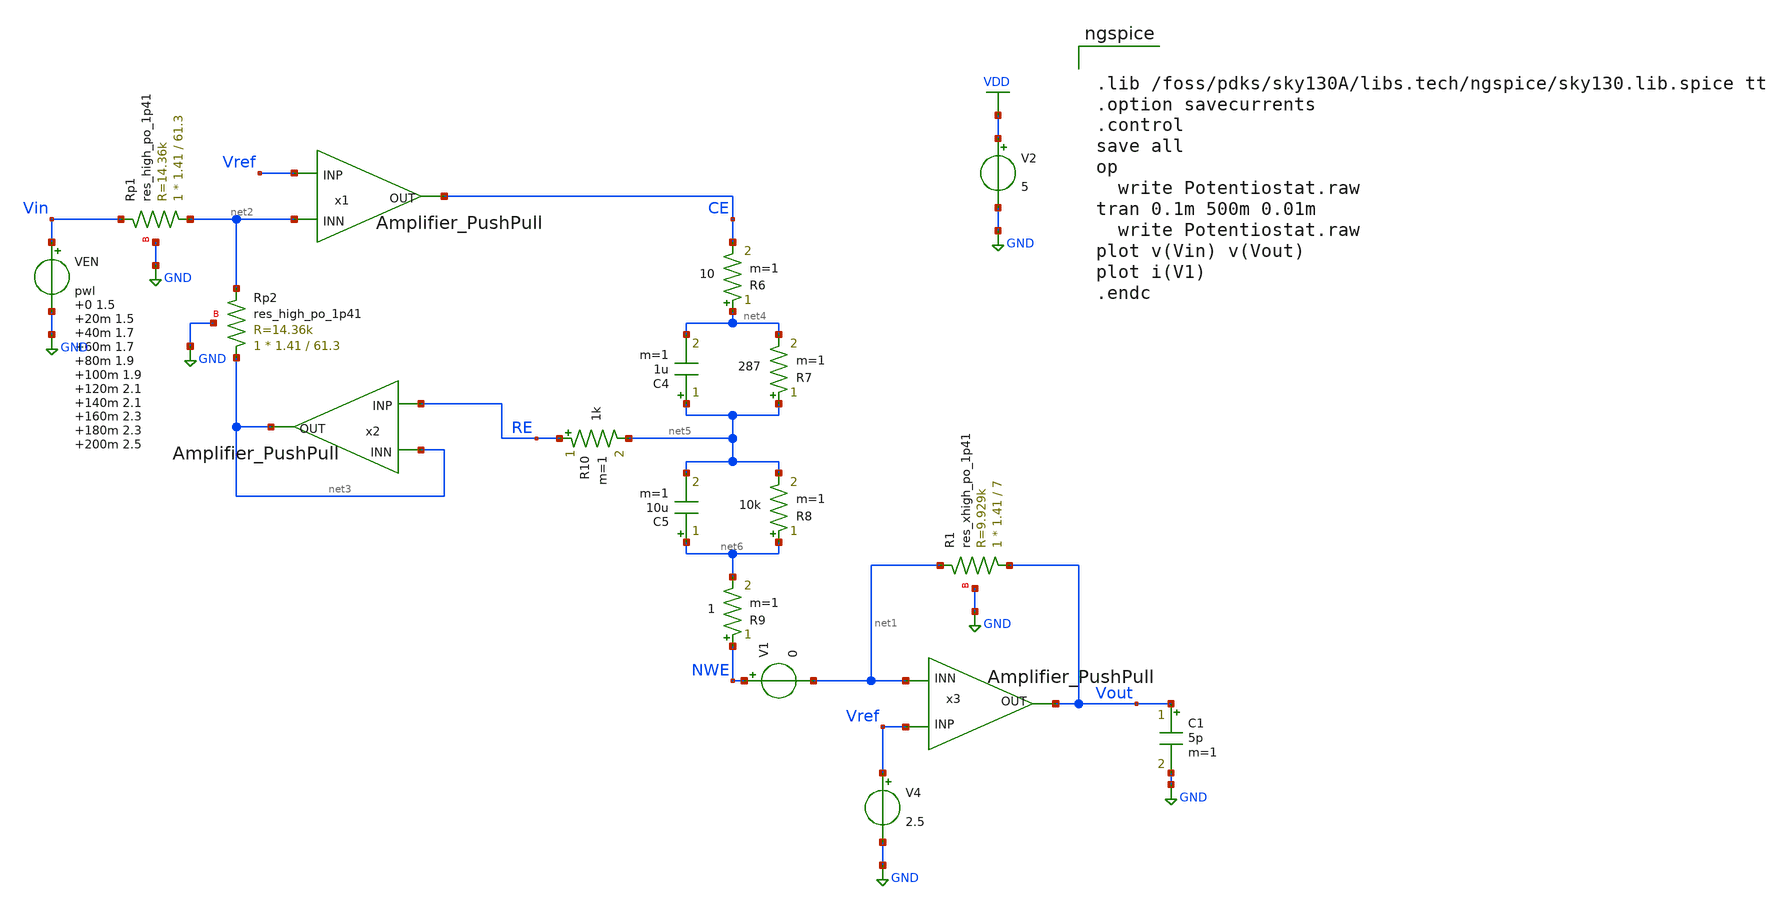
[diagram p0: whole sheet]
** sch_path: Potentiostat.sch
**.subckt Potentiostat
C1 Vout GND 5p m=1
V4 Vref GND 2.5
x3 Vout Vref net1 Amplifier_PushPull
x1 CE Vref net2 Amplifier_PushPull
XRp1 net2 Vin GND sky130_fd_pr__res_high_po_1p41 L=61.3 mult=1 m=1
XRp2 net3 net2 GND sky130_fd_pr__res_high_po_1p41 L=61.3 mult=1 m=1
x2 net3 RE net3 Amplifier_PushPull
R6 net4 CE 10 m=1
R7 net5 net4 287 m=1
C4 net5 net4 1u m=1
C5 net6 net5 10u m=1
R8 net6 net5 10k m=1
R9 NWE net6 1 m=1
R10 RE net5 1k m=1
V2 VDD GND 5
VEN Vin GND pwl 0 1.5 20m 1.5 40m 1.7 60m 1.7 80m 1.9 100m 1.9 120m 2.1 140m 2.1 160m 2.3 180m 2.3
+ 200m 2.5 220m 2.5 240m 2.7 260m 2.7 280m 2.9 300m 2.9 320m 3.1 340m 3.1 360m 3.3 380m 3.3 400m 3.5 420m
+ 3.5
V1 NWE net1 0
XR1 Vout net1 GND sky130_fd_pr__res_xhigh_po_1p41 L=7 mult=1 m=1
**** begin user architecture code


.lib /foss/pdks/sky130A/libs.tech/ngspice/sky130.lib.spice tt
.option savecurrents
.control
save all
op
  write Potentiostat.raw
tran 0.1m 500m 0.01m
  write Potentiostat.raw
plot v(Vin) v(Vout)
plot i(V1)
.endc


**** end user architecture code
**.ends

* expanding   symbol:  /foss/designs/Amplifier_PushPull.sym # of pins=3
** sym_path: Amplifier_PushPull.sym
** sch_path: Amplifier_PushPull.sch
.subckt Amplifier_PushPull OUT INP INN
*.ipin INN
*.opin OUT
*.ipin INP
XM1 net1 net1 GND GND sky130_fd_pr__nfet_g5v0d10v5 L=1.2 W=40 nf=4 ad='int((nf+1)/2) * W/nf * 0.29' as='int((nf+2)/2) * W/nf * 0.29'
+ pd='2*int((nf+1)/2) * (W/nf + 0.29)' ps='2*int((nf+2)/2) * (W/nf + 0.29)' nrd='0.29 / W' nrs='0.29 / W'
+ sa=0 sb=0 sd=0 mult=1 m=1
I0 VDD net1 64u
XM4 VBP VBP VDD VDD sky130_fd_pr__pfet_g5v0d10v5 L=1.2 W=48 nf=4 ad='int((nf+1)/2) * W/nf * 0.29' as='int((nf+2)/2) * W/nf * 0.29'
+ pd='2*int((nf+1)/2) * (W/nf + 0.29)' ps='2*int((nf+2)/2) * (W/nf + 0.29)' nrd='0.29 / W' nrs='0.29 / W'
+ sa=0 sb=0 sd=0 mult=1 m=1
XM5 VBP INN net3 GND sky130_fd_pr__nfet_g5v0d10v5 L=1.2 W=20 nf=2 ad='int((nf+1)/2) * W/nf * 0.29' as='int((nf+2)/2) * W/nf * 0.29'
+ pd='2*int((nf+1)/2) * (W/nf + 0.29)' ps='2*int((nf+2)/2) * (W/nf + 0.29)' nrd='0.29 / W' nrs='0.29 / W'
+ sa=0 sb=0 sd=0 mult=1 m=1
XM2 net3 net1 GND GND sky130_fd_pr__nfet_g5v0d10v5 L=1.2 W=40 nf=4 ad='int((nf+1)/2) * W/nf * 0.29' as='int((nf+2)/2) * W/nf * 0.29'
+ pd='2*int((nf+1)/2) * (W/nf + 0.29)' ps='2*int((nf+2)/2) * (W/nf + 0.29)' nrd='0.29 / W' nrs='0.29 / W'
+ sa=0 sb=0 sd=0 mult=1 m=1
XM3 net2 VBP VDD VDD sky130_fd_pr__pfet_g5v0d10v5 L=1.2 W=48 nf=4 ad='int((nf+1)/2) * W/nf * 0.29' as='int((nf+2)/2) * W/nf * 0.29'
+ pd='2*int((nf+1)/2) * (W/nf + 0.29)' ps='2*int((nf+2)/2) * (W/nf + 0.29)' nrd='0.29 / W' nrs='0.29 / W'
+ sa=0 sb=0 sd=0 mult=1 m=1
XM6 net2 INP net3 GND sky130_fd_pr__nfet_g5v0d10v5 L=1.2 W=20 nf=2 ad='int((nf+1)/2) * W/nf * 0.29' as='int((nf+2)/2) * W/nf * 0.29'
+ pd='2*int((nf+1)/2) * (W/nf + 0.29)' ps='2*int((nf+2)/2) * (W/nf + 0.29)' nrd='0.29 / W' nrs='0.29 / W'
+ sa=0 sb=0 sd=0 mult=1 m=1
XM7 net2 VBP VDD VDD sky130_fd_pr__pfet_g5v0d10v5 L=1.2 W=48 nf=4 ad='int((nf+1)/2) * W/nf * 0.29' as='int((nf+2)/2) * W/nf * 0.29'
+ pd='2*int((nf+1)/2) * (W/nf + 0.29)' ps='2*int((nf+2)/2) * (W/nf + 0.29)' nrd='0.29 / W' nrs='0.29 / W'
+ sa=0 sb=0 sd=0 mult=1 m=1
XM8 net4 VCasP net2 VDD sky130_fd_pr__pfet_g5v0d10v5 L=1.2 W=24 nf=4 ad='int((nf+1)/2) * W/nf * 0.29'
+ as='int((nf+2)/2) * W/nf * 0.29' pd='2*int((nf+1)/2) * (W/nf + 0.29)' ps='2*int((nf+2)/2) * (W/nf + 0.29)'
+ nrd='0.29 / W' nrs='0.29 / W' sa=0 sb=0 sd=0 mult=1 m=1
XM9 OUT net2 VDD VDD sky130_fd_pr__pfet_g5v0d10v5 L=1.2 W=96 nf=8 ad='int((nf+1)/2) * W/nf * 0.29' as='int((nf+2)/2) * W/nf * 0.29'
+ pd='2*int((nf+1)/2) * (W/nf + 0.29)' ps='2*int((nf+2)/2) * (W/nf + 0.29)' nrd='0.29 / W' nrs='0.29 / W'
+ sa=0 sb=0 sd=0 mult=1 m=1
XM10 net2 VCasN net4 GND sky130_fd_pr__nfet_g5v0d10v5 L=1.2 W=10 nf=2 ad='int((nf+1)/2) * W/nf * 0.29'
+ as='int((nf+2)/2) * W/nf * 0.29' pd='2*int((nf+1)/2) * (W/nf + 0.29)' ps='2*int((nf+2)/2) * (W/nf + 0.29)'
+ nrd='0.29 / W' nrs='0.29 / W' sa=0 sb=0 sd=0 mult=1 m=1
XM11 net4 net1 GND GND sky130_fd_pr__nfet_g5v0d10v5 L=1.2 W=20 nf=2 ad='int((nf+1)/2) * W/nf * 0.29'
+ as='int((nf+2)/2) * W/nf * 0.29' pd='2*int((nf+1)/2) * (W/nf + 0.29)' ps='2*int((nf+2)/2) * (W/nf + 0.29)'
+ nrd='0.29 / W' nrs='0.29 / W' sa=0 sb=0 sd=0 mult=1 m=1
XM12 OUT net4 GND GND sky130_fd_pr__nfet_g5v0d10v5 L=1.2 W=40 nf=4 ad='int((nf+1)/2) * W/nf * 0.29' as='int((nf+2)/2) * W/nf * 0.29'
+ pd='2*int((nf+1)/2) * (W/nf + 0.29)' ps='2*int((nf+2)/2) * (W/nf + 0.29)' nrd='0.29 / W' nrs='0.29 / W'
+ sa=0 sb=0 sd=0 mult=1 m=1
XR3 net5 net2 GND sky130_fd_pr__res_high_po_1p41 L=9.9 mult=1 m=1
XC1 net5 OUT sky130_fd_pr__cap_mim_m3_1 W=16 L=16 MF=4 m=4
XM16 VCasP net1 GND GND sky130_fd_pr__nfet_g5v0d10v5 L=1.2 W=20 nf=2 ad='int((nf+1)/2) * W/nf * 0.29'
+ as='int((nf+2)/2) * W/nf * 0.29' pd='2*int((nf+1)/2) * (W/nf + 0.29)' ps='2*int((nf+2)/2) * (W/nf + 0.29)'
+ nrd='0.29 / W' nrs='0.29 / W' sa=0 sb=0 sd=0 mult=1 m=1
XM17 VCasP VCasP net7 VDD sky130_fd_pr__pfet_g5v0d10v5 L=1.2 W=48 nf=4 ad='int((nf+1)/2) * W/nf * 0.29'
+ as='int((nf+2)/2) * W/nf * 0.29' pd='2*int((nf+1)/2) * (W/nf + 0.29)' ps='2*int((nf+2)/2) * (W/nf + 0.29)'
+ nrd='0.29 / W' nrs='0.29 / W' sa=0 sb=0 sd=0 mult=1 m=1
XM18 net7 net7 VDD VDD sky130_fd_pr__pfet_g5v0d10v5 L=1.2 W=48 nf=4 ad='int((nf+1)/2) * W/nf * 0.29'
+ as='int((nf+2)/2) * W/nf * 0.29' pd='2*int((nf+1)/2) * (W/nf + 0.29)' ps='2*int((nf+2)/2) * (W/nf + 0.29)'
+ nrd='0.29 / W' nrs='0.29 / W' sa=0 sb=0 sd=0 mult=1 m=1
XM19 net6 net6 GND GND sky130_fd_pr__nfet_g5v0d10v5 L=1.2 W=20 nf=2 ad='int((nf+1)/2) * W/nf * 0.29'
+ as='int((nf+2)/2) * W/nf * 0.29' pd='2*int((nf+1)/2) * (W/nf + 0.29)' ps='2*int((nf+2)/2) * (W/nf + 0.29)'
+ nrd='0.29 / W' nrs='0.29 / W' sa=0 sb=0 sd=0 mult=1 m=1
XM20 VCasN VCasN net6 GND sky130_fd_pr__nfet_g5v0d10v5 L=1.2 W=20 nf=2 ad='int((nf+1)/2) * W/nf * 0.29'
+ as='int((nf+2)/2) * W/nf * 0.29' pd='2*int((nf+1)/2) * (W/nf + 0.29)' ps='2*int((nf+2)/2) * (W/nf + 0.29)'
+ nrd='0.29 / W' nrs='0.29 / W' sa=0 sb=0 sd=0 mult=1 m=1
XM21 VCasN VBP VDD VDD sky130_fd_pr__pfet_g5v0d10v5 L=1.2 W=48 nf=4 ad='int((nf+1)/2) * W/nf * 0.29'
+ as='int((nf+2)/2) * W/nf * 0.29' pd='2*int((nf+1)/2) * (W/nf + 0.29)' ps='2*int((nf+2)/2) * (W/nf + 0.29)'
+ nrd='0.29 / W' nrs='0.29 / W' sa=0 sb=0 sd=0 mult=1 m=1
.ends

.GLOBAL GND
.GLOBAL VDD
.end
